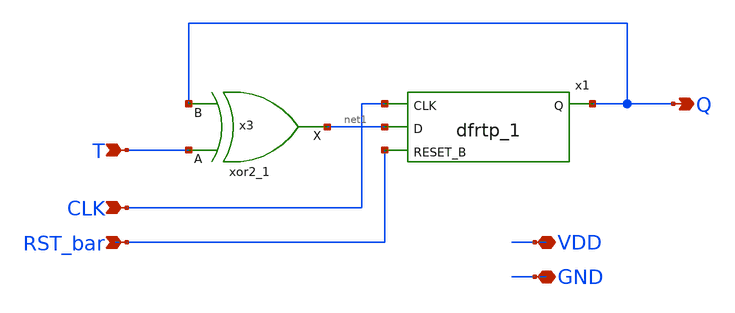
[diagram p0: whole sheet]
** sch_path: xschem/T_flip_flop/asyn_rst_t_ff.sch
**.subckt asyn_rst_t_ff T CLK Q RST_bar VDD GND
*.ipin T
*.ipin CLK
*.opin Q
*.ipin RST_bar
*.iopin VDD
*.iopin GND
x1 CLK net1 RST_bar GND GND VDD VDD Q sky130_fd_sc_lp__dfrtp_1
x3 T Q GND GND VDD VDD net1 sky130_fd_sc_lp__xor2_1
**.ends
.end
